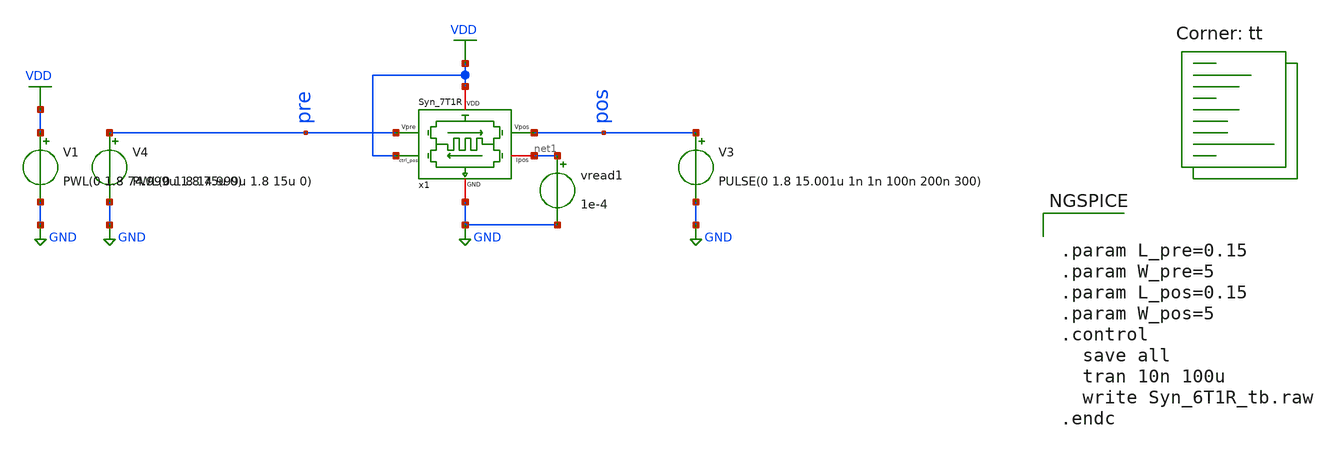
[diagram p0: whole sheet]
** sch_path: SNN/Syn_7T1R_tb.sch
**.subckt Syn_7T1R_tb
V1 VDD GND PWL(0 1.8 74.999u 1.8 75u 0)
V3 pos GND PULSE(0 1.8 15.001u 1n 1n 100n 200n 300)
vread1 net1 GND 1e-4
V4 pre GND PWL(0 1.8 14.999u 1.8 15u 0)
x1 VDD VDD net1 pre pos GND Syn_7T1R
**** begin user architecture code
.lib $::SKYWATER_MODELS/sky130.lib.spice tt

** opencircuitdesign pdks install
.inc $::SKYWATER_MODELS/rram_v0.spice



.param L_pre=0.15
.param W_pre=5
.param L_pos=0.15
.param W_pos=5
.control
  save all
  tran 10n 100u
  write Syn_6T1R_tb.raw
.endc


**** end user architecture code
**.ends
.GLOBAL GND
.GLOBAL VDD
.end
